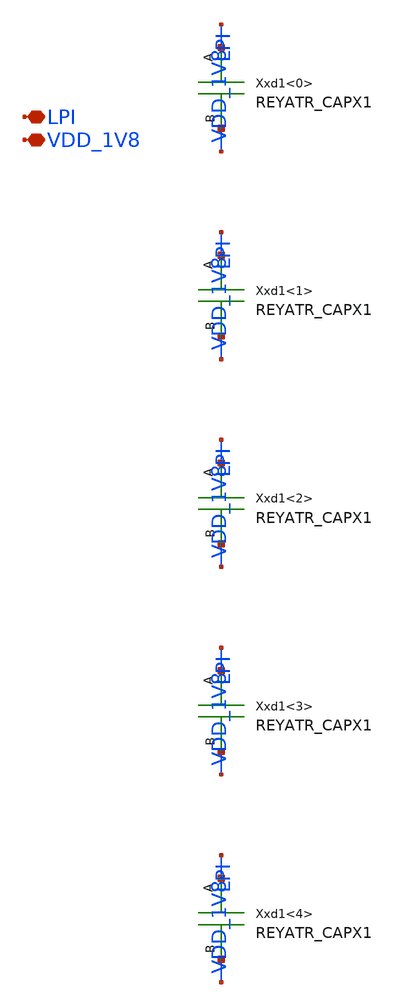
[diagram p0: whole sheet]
** sch_path: design/LELO_TEMP_SKY130A/LELOTEMP_BIAS_IBP_CAP_LPI_A.sch
**.subckt LELOTEMP_BIAS_IBP_CAP_LPI_A LPI VDD_1V8
*.iopin LPI
*.iopin VDD_1V8
Xxd1<0> LPI VDD_1V8 REYATR_CAPX1
Xxd1<1> LPI VDD_1V8 REYATR_CAPX1
Xxd1<2> LPI VDD_1V8 REYATR_CAPX1
Xxd1<3> LPI VDD_1V8 REYATR_CAPX1
Xxd1<4> LPI VDD_1V8 REYATR_CAPX1
**.ends

* expanding   symbol:  REY_ATR_SKY130A/REYATR_CAPX1.sym # of pins=2
** sym_path: design/LELO_TEMP_SKY130A/REYATR_CAPX1.sym
** sch_path: design/LELO_TEMP_SKY130A/REYATR_CAPX1.sch
.subckt REYATR_CAPX1 A B
*.iopin A
*.iopin B
XC1 B A sky130_fd_pr__cap_mim_m3_1 W=4.8 L=5 MF=1 m=1
.ends

.end
